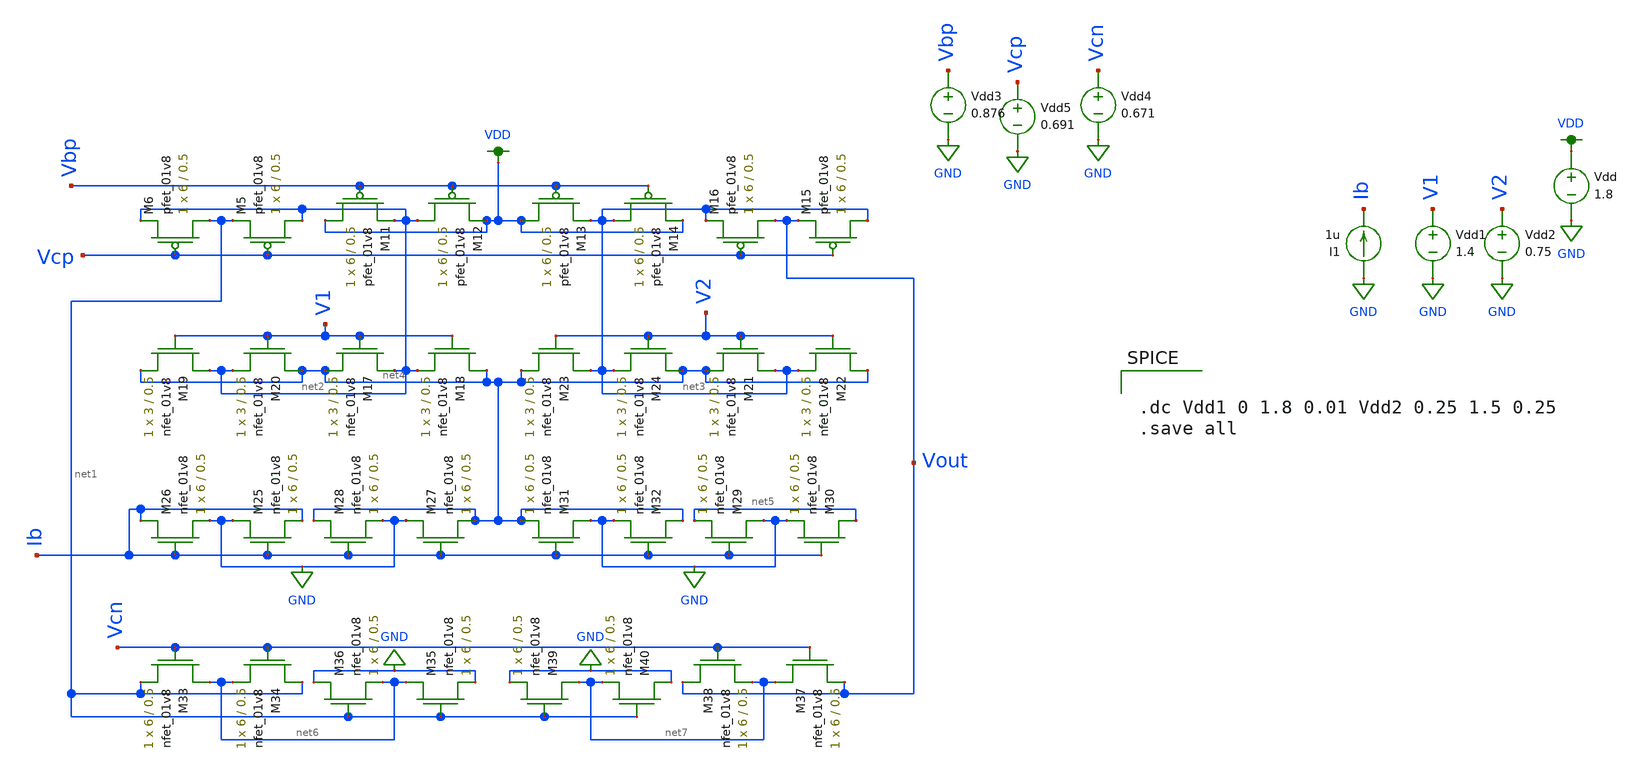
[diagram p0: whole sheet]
** sch_path: mp3/schematic/amp2.sch
**.subckt amp2
XM5 net2 Vcp net1 VDD sky130_fd_pr__pfet_01v8 L=0.5 W=6 nf=1 ad='int((nf+1)/2) * W/nf * 0.29' as='int((nf+2)/2) * W/nf * 0.29'
+ pd='2*int((nf+1)/2) * (W/nf + 0.29)' ps='2*int((nf+2)/2) * (W/nf + 0.29)' nrd='0.29 / W' nrs='0.29 / W'
+ sa=0 sb=0 sd=0 mult=1 m=1
XM6 net1 Vcp net2 VDD sky130_fd_pr__pfet_01v8 L=0.5 W=6 nf=1 ad='int((nf+1)/2) * W/nf * 0.29' as='int((nf+2)/2) * W/nf * 0.29'
+ pd='2*int((nf+1)/2) * (W/nf + 0.29)' ps='2*int((nf+2)/2) * (W/nf + 0.29)' nrd='0.29 / W' nrs='0.29 / W'
+ sa=0 sb=0 sd=0 mult=1 m=1
XM11 VDD Vbp net2 VDD sky130_fd_pr__pfet_01v8 L=0.5 W=6 nf=1 ad='int((nf+1)/2) * W/nf * 0.29' as='int((nf+2)/2) * W/nf * 0.29'
+ pd='2*int((nf+1)/2) * (W/nf + 0.29)' ps='2*int((nf+2)/2) * (W/nf + 0.29)' nrd='0.29 / W' nrs='0.29 / W'
+ sa=0 sb=0 sd=0 mult=1 m=1
XM12 net2 Vbp VDD VDD sky130_fd_pr__pfet_01v8 L=0.5 W=6 nf=1 ad='int((nf+1)/2) * W/nf * 0.29' as='int((nf+2)/2) * W/nf * 0.29'
+ pd='2*int((nf+1)/2) * (W/nf + 0.29)' ps='2*int((nf+2)/2) * (W/nf + 0.29)' nrd='0.29 / W' nrs='0.29 / W'
+ sa=0 sb=0 sd=0 mult=1 m=1
XM13 VDD Vbp net3 VDD sky130_fd_pr__pfet_01v8 L=0.5 W=6 nf=1 ad='int((nf+1)/2) * W/nf * 0.29' as='int((nf+2)/2) * W/nf * 0.29'
+ pd='2*int((nf+1)/2) * (W/nf + 0.29)' ps='2*int((nf+2)/2) * (W/nf + 0.29)' nrd='0.29 / W' nrs='0.29 / W'
+ sa=0 sb=0 sd=0 mult=1 m=1
XM14 net3 Vbp VDD VDD sky130_fd_pr__pfet_01v8 L=0.5 W=6 nf=1 ad='int((nf+1)/2) * W/nf * 0.29' as='int((nf+2)/2) * W/nf * 0.29'
+ pd='2*int((nf+1)/2) * (W/nf + 0.29)' ps='2*int((nf+2)/2) * (W/nf + 0.29)' nrd='0.29 / W' nrs='0.29 / W'
+ sa=0 sb=0 sd=0 mult=1 m=1
XM15 net3 Vcp Vout VDD sky130_fd_pr__pfet_01v8 L=0.5 W=6 nf=1 ad='int((nf+1)/2) * W/nf * 0.29' as='int((nf+2)/2) * W/nf * 0.29'
+ pd='2*int((nf+1)/2) * (W/nf + 0.29)' ps='2*int((nf+2)/2) * (W/nf + 0.29)' nrd='0.29 / W' nrs='0.29 / W'
+ sa=0 sb=0 sd=0 mult=1 m=1
XM16 Vout Vcp net3 VDD sky130_fd_pr__pfet_01v8 L=0.5 W=6 nf=1 ad='int((nf+1)/2) * W/nf * 0.29' as='int((nf+2)/2) * W/nf * 0.29'
+ pd='2*int((nf+1)/2) * (W/nf + 0.29)' ps='2*int((nf+2)/2) * (W/nf + 0.29)' nrd='0.29 / W' nrs='0.29 / W'
+ sa=0 sb=0 sd=0 mult=1 m=1
XM17 net2 V1 net4 GND sky130_fd_pr__nfet_01v8 L=0.5 W=3 nf=1 ad='int((nf+1)/2) * W/nf * 0.29' as='int((nf+2)/2) * W/nf * 0.29'
+ pd='2*int((nf+1)/2) * (W/nf + 0.29)' ps='2*int((nf+2)/2) * (W/nf + 0.29)' nrd='0.29 / W' nrs='0.29 / W'
+ sa=0 sb=0 sd=0 mult=1 m=1
XM18 net4 V1 net2 GND sky130_fd_pr__nfet_01v8 L=0.5 W=3 nf=1 ad='int((nf+1)/2) * W/nf * 0.29' as='int((nf+2)/2) * W/nf * 0.29'
+ pd='2*int((nf+1)/2) * (W/nf + 0.29)' ps='2*int((nf+2)/2) * (W/nf + 0.29)' nrd='0.29 / W' nrs='0.29 / W'
+ sa=0 sb=0 sd=0 mult=1 m=1
XM19 net2 V1 net4 GND sky130_fd_pr__nfet_01v8 L=0.5 W=3 nf=1 ad='int((nf+1)/2) * W/nf * 0.29' as='int((nf+2)/2) * W/nf * 0.29'
+ pd='2*int((nf+1)/2) * (W/nf + 0.29)' ps='2*int((nf+2)/2) * (W/nf + 0.29)' nrd='0.29 / W' nrs='0.29 / W'
+ sa=0 sb=0 sd=0 mult=1 m=1
XM20 net4 V1 net2 GND sky130_fd_pr__nfet_01v8 L=0.5 W=3 nf=1 ad='int((nf+1)/2) * W/nf * 0.29' as='int((nf+2)/2) * W/nf * 0.29'
+ pd='2*int((nf+1)/2) * (W/nf + 0.29)' ps='2*int((nf+2)/2) * (W/nf + 0.29)' nrd='0.29 / W' nrs='0.29 / W'
+ sa=0 sb=0 sd=0 mult=1 m=1
XM21 net3 V2 net4 GND sky130_fd_pr__nfet_01v8 L=0.5 W=3 nf=1 ad='int((nf+1)/2) * W/nf * 0.29' as='int((nf+2)/2) * W/nf * 0.29'
+ pd='2*int((nf+1)/2) * (W/nf + 0.29)' ps='2*int((nf+2)/2) * (W/nf + 0.29)' nrd='0.29 / W' nrs='0.29 / W'
+ sa=0 sb=0 sd=0 mult=1 m=1
XM22 net4 V2 net3 GND sky130_fd_pr__nfet_01v8 L=0.5 W=3 nf=1 ad='int((nf+1)/2) * W/nf * 0.29' as='int((nf+2)/2) * W/nf * 0.29'
+ pd='2*int((nf+1)/2) * (W/nf + 0.29)' ps='2*int((nf+2)/2) * (W/nf + 0.29)' nrd='0.29 / W' nrs='0.29 / W'
+ sa=0 sb=0 sd=0 mult=1 m=1
XM23 net3 V2 net4 GND sky130_fd_pr__nfet_01v8 L=0.5 W=3 nf=1 ad='int((nf+1)/2) * W/nf * 0.29' as='int((nf+2)/2) * W/nf * 0.29'
+ pd='2*int((nf+1)/2) * (W/nf + 0.29)' ps='2*int((nf+2)/2) * (W/nf + 0.29)' nrd='0.29 / W' nrs='0.29 / W'
+ sa=0 sb=0 sd=0 mult=1 m=1
XM24 net4 V2 net3 GND sky130_fd_pr__nfet_01v8 L=0.5 W=3 nf=1 ad='int((nf+1)/2) * W/nf * 0.29' as='int((nf+2)/2) * W/nf * 0.29'
+ pd='2*int((nf+1)/2) * (W/nf + 0.29)' ps='2*int((nf+2)/2) * (W/nf + 0.29)' nrd='0.29 / W' nrs='0.29 / W'
+ sa=0 sb=0 sd=0 mult=1 m=1
XM25 GND Ib Ib GND sky130_fd_pr__nfet_01v8 L=0.5 W=6 nf=1 ad='int((nf+1)/2) * W/nf * 0.29' as='int((nf+2)/2) * W/nf * 0.29'
+ pd='2*int((nf+1)/2) * (W/nf + 0.29)' ps='2*int((nf+2)/2) * (W/nf + 0.29)' nrd='0.29 / W' nrs='0.29 / W'
+ sa=0 sb=0 sd=0 mult=1 m=1
XM26 Ib Ib GND GND sky130_fd_pr__nfet_01v8 L=0.5 W=6 nf=1 ad='int((nf+1)/2) * W/nf * 0.29' as='int((nf+2)/2) * W/nf * 0.29'
+ pd='2*int((nf+1)/2) * (W/nf + 0.29)' ps='2*int((nf+2)/2) * (W/nf + 0.29)' nrd='0.29 / W' nrs='0.29 / W'
+ sa=0 sb=0 sd=0 mult=1 m=1
XM27 GND Ib net4 GND sky130_fd_pr__nfet_01v8 L=0.5 W=6 nf=1 ad='int((nf+1)/2) * W/nf * 0.29' as='int((nf+2)/2) * W/nf * 0.29'
+ pd='2*int((nf+1)/2) * (W/nf + 0.29)' ps='2*int((nf+2)/2) * (W/nf + 0.29)' nrd='0.29 / W' nrs='0.29 / W'
+ sa=0 sb=0 sd=0 mult=1 m=1
XM28 net4 Ib GND GND sky130_fd_pr__nfet_01v8 L=0.5 W=6 nf=1 ad='int((nf+1)/2) * W/nf * 0.29' as='int((nf+2)/2) * W/nf * 0.29'
+ pd='2*int((nf+1)/2) * (W/nf + 0.29)' ps='2*int((nf+2)/2) * (W/nf + 0.29)' nrd='0.29 / W' nrs='0.29 / W'
+ sa=0 sb=0 sd=0 mult=1 m=1
XM29 GND Ib net5 GND sky130_fd_pr__nfet_01v8 L=0.5 W=6 nf=1 ad='int((nf+1)/2) * W/nf * 0.29' as='int((nf+2)/2) * W/nf * 0.29'
+ pd='2*int((nf+1)/2) * (W/nf + 0.29)' ps='2*int((nf+2)/2) * (W/nf + 0.29)' nrd='0.29 / W' nrs='0.29 / W'
+ sa=0 sb=0 sd=0 mult=1 m=1
XM30 net5 Ib GND GND sky130_fd_pr__nfet_01v8 L=0.5 W=6 nf=1 ad='int((nf+1)/2) * W/nf * 0.29' as='int((nf+2)/2) * W/nf * 0.29'
+ pd='2*int((nf+1)/2) * (W/nf + 0.29)' ps='2*int((nf+2)/2) * (W/nf + 0.29)' nrd='0.29 / W' nrs='0.29 / W'
+ sa=0 sb=0 sd=0 mult=1 m=1
XM31 GND Ib net4 GND sky130_fd_pr__nfet_01v8 L=0.5 W=6 nf=1 ad='int((nf+1)/2) * W/nf * 0.29' as='int((nf+2)/2) * W/nf * 0.29'
+ pd='2*int((nf+1)/2) * (W/nf + 0.29)' ps='2*int((nf+2)/2) * (W/nf + 0.29)' nrd='0.29 / W' nrs='0.29 / W'
+ sa=0 sb=0 sd=0 mult=1 m=1
XM32 net4 Ib GND GND sky130_fd_pr__nfet_01v8 L=0.5 W=6 nf=1 ad='int((nf+1)/2) * W/nf * 0.29' as='int((nf+2)/2) * W/nf * 0.29'
+ pd='2*int((nf+1)/2) * (W/nf + 0.29)' ps='2*int((nf+2)/2) * (W/nf + 0.29)' nrd='0.29 / W' nrs='0.29 / W'
+ sa=0 sb=0 sd=0 mult=1 m=1
XM33 net6 Vcn net1 GND sky130_fd_pr__nfet_01v8 L=0.5 W=6 nf=1 ad='int((nf+1)/2) * W/nf * 0.29' as='int((nf+2)/2) * W/nf * 0.29'
+ pd='2*int((nf+1)/2) * (W/nf + 0.29)' ps='2*int((nf+2)/2) * (W/nf + 0.29)' nrd='0.29 / W' nrs='0.29 / W'
+ sa=0 sb=0 sd=0 mult=1 m=1
XM34 net1 Vcn net6 GND sky130_fd_pr__nfet_01v8 L=0.5 W=6 nf=1 ad='int((nf+1)/2) * W/nf * 0.29' as='int((nf+2)/2) * W/nf * 0.29'
+ pd='2*int((nf+1)/2) * (W/nf + 0.29)' ps='2*int((nf+2)/2) * (W/nf + 0.29)' nrd='0.29 / W' nrs='0.29 / W'
+ sa=0 sb=0 sd=0 mult=1 m=1
XM35 net6 net1 GND GND sky130_fd_pr__nfet_01v8 L=0.5 W=6 nf=1 ad='int((nf+1)/2) * W/nf * 0.29' as='int((nf+2)/2) * W/nf * 0.29'
+ pd='2*int((nf+1)/2) * (W/nf + 0.29)' ps='2*int((nf+2)/2) * (W/nf + 0.29)' nrd='0.29 / W' nrs='0.29 / W'
+ sa=0 sb=0 sd=0 mult=1 m=1
XM36 GND net1 net6 GND sky130_fd_pr__nfet_01v8 L=0.5 W=6 nf=1 ad='int((nf+1)/2) * W/nf * 0.29' as='int((nf+2)/2) * W/nf * 0.29'
+ pd='2*int((nf+1)/2) * (W/nf + 0.29)' ps='2*int((nf+2)/2) * (W/nf + 0.29)' nrd='0.29 / W' nrs='0.29 / W'
+ sa=0 sb=0 sd=0 mult=1 m=1
XM37 net7 Vcn Vout GND sky130_fd_pr__nfet_01v8 L=0.5 W=6 nf=1 ad='int((nf+1)/2) * W/nf * 0.29' as='int((nf+2)/2) * W/nf * 0.29'
+ pd='2*int((nf+1)/2) * (W/nf + 0.29)' ps='2*int((nf+2)/2) * (W/nf + 0.29)' nrd='0.29 / W' nrs='0.29 / W'
+ sa=0 sb=0 sd=0 mult=1 m=1
XM38 Vout Vcn net7 GND sky130_fd_pr__nfet_01v8 L=0.5 W=6 nf=1 ad='int((nf+1)/2) * W/nf * 0.29' as='int((nf+2)/2) * W/nf * 0.29'
+ pd='2*int((nf+1)/2) * (W/nf + 0.29)' ps='2*int((nf+2)/2) * (W/nf + 0.29)' nrd='0.29 / W' nrs='0.29 / W'
+ sa=0 sb=0 sd=0 mult=1 m=1
XM39 net7 net1 GND GND sky130_fd_pr__nfet_01v8 L=0.5 W=6 nf=1 ad='int((nf+1)/2) * W/nf * 0.29' as='int((nf+2)/2) * W/nf * 0.29'
+ pd='2*int((nf+1)/2) * (W/nf + 0.29)' ps='2*int((nf+2)/2) * (W/nf + 0.29)' nrd='0.29 / W' nrs='0.29 / W'
+ sa=0 sb=0 sd=0 mult=1 m=1
XM40 GND net1 net7 GND sky130_fd_pr__nfet_01v8 L=0.5 W=6 nf=1 ad='int((nf+1)/2) * W/nf * 0.29' as='int((nf+2)/2) * W/nf * 0.29'
+ pd='2*int((nf+1)/2) * (W/nf + 0.29)' ps='2*int((nf+2)/2) * (W/nf + 0.29)' nrd='0.29 / W' nrs='0.29 / W'
+ sa=0 sb=0 sd=0 mult=1 m=1
Vdd1 V1 GND 1.4
Vdd2 V2 GND 0.75
I1 GND Ib 1u
Vdd VDD GND 1.8
Vdd3 Vbp GND 0.876
Vdd4 Vcn GND 0.671
Vdd5 Vcp GND 0.691
**** begin user architecture code

.option wnflag=1
.lib ~/skywater/skywater-pdk/libraries/sky130_fd_pr_ngspice/latest/models/sky130.lib.spice tt



.dc Vdd1 0 1.8 0.01 Vdd2 0.25 1.5 0.25
.save all

**** end user architecture code
**.ends
.GLOBAL GND
.GLOBAL VDD
.end
